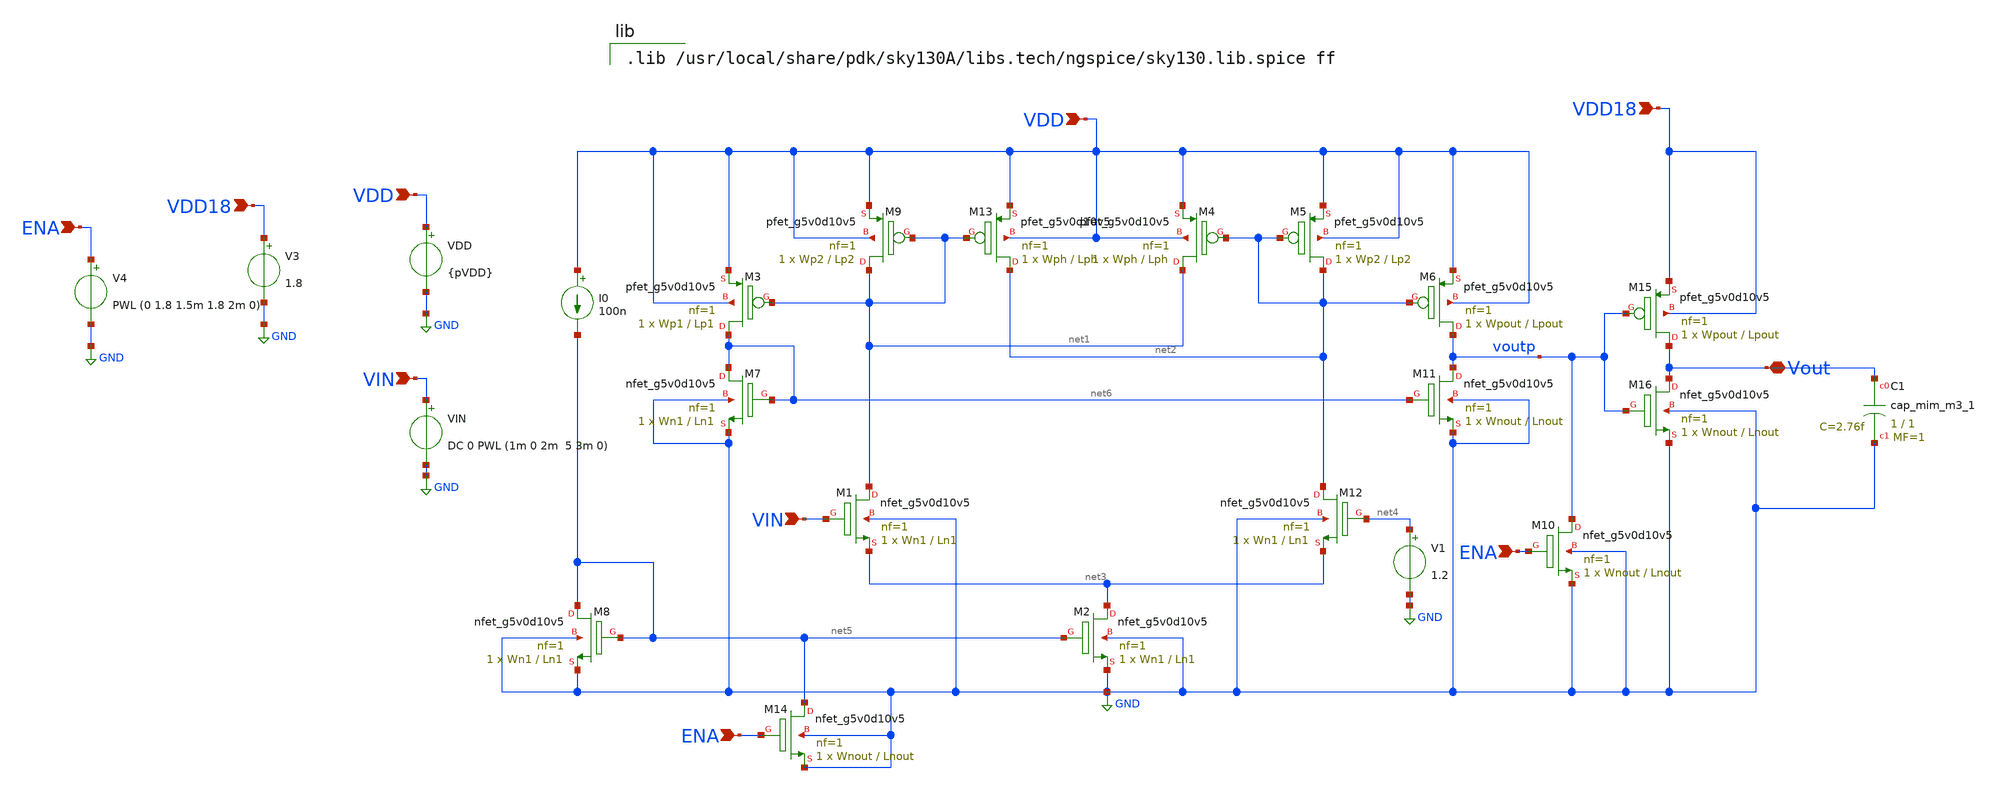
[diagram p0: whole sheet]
** sch_path: xschem/Comparador_Final.sch
**.subckt Comparador_Final VDD VDD Vout VIN VIN VDD18 VDD18 ENA ENA ENA
*.ipin VDD
*.ipin VDD
*.iopin Vout
*.ipin VIN
*.ipin VIN
*.ipin VDD18
*.ipin VDD18
*.ipin ENA
*.ipin ENA
*.ipin ENA
V1 net4 GND 1.2
VDD VDD GND {pVDD}
VIN VIN GND DC 0 PWL (1m 0 2m 5 3m 0)
I0 VDD net5 100n
XM3 net6 net1 VDD VDD sky130_fd_pr__pfet_g5v0d10v5 L=Lp1 W=Wp1 nf=1 ad='int((nf+1)/2) * W/nf * 0.29'
+ as='int((nf+2)/2) * W/nf * 0.29' pd='2*int((nf+1)/2) * (W/nf + 0.29)' ps='2*int((nf+2)/2) * (W/nf + 0.29)'
+ nrd='0.29 / W' nrs='0.29 / W' sa=0 sb=0 sd=0 mult=1 m=1
XM9 net1 net1 VDD VDD sky130_fd_pr__pfet_g5v0d10v5 L=Lp2 W=Wp2 nf=1 ad='int((nf+1)/2) * W/nf * 0.29'
+ as='int((nf+2)/2) * W/nf * 0.29' pd='2*int((nf+1)/2) * (W/nf + 0.29)' ps='2*int((nf+2)/2) * (W/nf + 0.29)'
+ nrd='0.29 / W' nrs='0.29 / W' sa=0 sb=0 sd=0 mult=1 m=1
XM13 net2 net1 VDD VDD sky130_fd_pr__pfet_g5v0d10v5 L=Lph W=Wph nf=1 ad='int((nf+1)/2) * W/nf * 0.29'
+ as='int((nf+2)/2) * W/nf * 0.29' pd='2*int((nf+1)/2) * (W/nf + 0.29)' ps='2*int((nf+2)/2) * (W/nf + 0.29)'
+ nrd='0.29 / W' nrs='0.29 / W' sa=0 sb=0 sd=0 mult=1 m=1
XM4 net1 net2 VDD VDD sky130_fd_pr__pfet_g5v0d10v5 L=Lph W=Wph nf=1 ad='int((nf+1)/2) * W/nf * 0.29'
+ as='int((nf+2)/2) * W/nf * 0.29' pd='2*int((nf+1)/2) * (W/nf + 0.29)' ps='2*int((nf+2)/2) * (W/nf + 0.29)'
+ nrd='0.29 / W' nrs='0.29 / W' sa=0 sb=0 sd=0 mult=1 m=1
XM5 net2 net2 VDD VDD sky130_fd_pr__pfet_g5v0d10v5 L=Lp2 W=Wp2 nf=1 ad='int((nf+1)/2) * W/nf * 0.29'
+ as='int((nf+2)/2) * W/nf * 0.29' pd='2*int((nf+1)/2) * (W/nf + 0.29)' ps='2*int((nf+2)/2) * (W/nf + 0.29)'
+ nrd='0.29 / W' nrs='0.29 / W' sa=0 sb=0 sd=0 mult=1 m=1
XM6 voutp net2 VDD VDD sky130_fd_pr__pfet_g5v0d10v5 L=Lpout W=Wpout nf=1 ad='int((nf+1)/2) * W/nf * 0.29'
+ as='int((nf+2)/2) * W/nf * 0.29' pd='2*int((nf+1)/2) * (W/nf + 0.29)' ps='2*int((nf+2)/2) * (W/nf + 0.29)'
+ nrd='0.29 / W' nrs='0.29 / W' sa=0 sb=0 sd=0 mult=1 m=1
XM11 voutp net6 GND GND sky130_fd_pr__nfet_g5v0d10v5 L=Lnout W=Wnout nf=1 ad='int((nf+1)/2) * W/nf * 0.29'
+ as='int((nf+2)/2) * W/nf * 0.29' pd='2*int((nf+1)/2) * (W/nf + 0.29)' ps='2*int((nf+2)/2) * (W/nf + 0.29)'
+ nrd='0.29 / W' nrs='0.29 / W' sa=0 sb=0 sd=0 mult=1 m=1
XM12 net2 net4 net3 GND sky130_fd_pr__nfet_g5v0d10v5 L=Ln1 W=Wn1 nf=1 ad='int((nf+1)/2) * W/nf * 0.29'
+ as='int((nf+2)/2) * W/nf * 0.29' pd='2*int((nf+1)/2) * (W/nf + 0.29)' ps='2*int((nf+2)/2) * (W/nf + 0.29)'
+ nrd='0.29 / W' nrs='0.29 / W' sa=0 sb=0 sd=0 mult=1 m=1
XM2 net3 net5 GND GND sky130_fd_pr__nfet_g5v0d10v5 L=Ln1 W=Wn1 nf=1 ad='int((nf+1)/2) * W/nf * 0.29'
+ as='int((nf+2)/2) * W/nf * 0.29' pd='2*int((nf+1)/2) * (W/nf + 0.29)' ps='2*int((nf+2)/2) * (W/nf + 0.29)'
+ nrd='0.29 / W' nrs='0.29 / W' sa=0 sb=0 sd=0 mult=1 m=1
XM1 net1 VIN net3 GND sky130_fd_pr__nfet_g5v0d10v5 L=Ln1 W=Wn1 nf=1 ad='int((nf+1)/2) * W/nf * 0.29'
+ as='int((nf+2)/2) * W/nf * 0.29' pd='2*int((nf+1)/2) * (W/nf + 0.29)' ps='2*int((nf+2)/2) * (W/nf + 0.29)'
+ nrd='0.29 / W' nrs='0.29 / W' sa=0 sb=0 sd=0 mult=1 m=1
XM7 net6 net6 GND GND sky130_fd_pr__nfet_g5v0d10v5 L=Ln1 W=Wn1 nf=1 ad='int((nf+1)/2) * W/nf * 0.29'
+ as='int((nf+2)/2) * W/nf * 0.29' pd='2*int((nf+1)/2) * (W/nf + 0.29)' ps='2*int((nf+2)/2) * (W/nf + 0.29)'
+ nrd='0.29 / W' nrs='0.29 / W' sa=0 sb=0 sd=0 mult=1 m=1
XM8 net5 net5 GND GND sky130_fd_pr__nfet_g5v0d10v5 L=Ln1 W=Wn1 nf=1 ad='int((nf+1)/2) * W/nf * 0.29'
+ as='int((nf+2)/2) * W/nf * 0.29' pd='2*int((nf+1)/2) * (W/nf + 0.29)' ps='2*int((nf+2)/2) * (W/nf + 0.29)'
+ nrd='0.29 / W' nrs='0.29 / W' sa=0 sb=0 sd=0 mult=1 m=1
V3 VDD18 GND 1.8
XM15 Vout voutp VDD18 VDD18 sky130_fd_pr__pfet_g5v0d10v5 L=Lpout W=Wpout nf=1 ad='int((nf+1)/2) * W/nf * 0.29'
+ as='int((nf+2)/2) * W/nf * 0.29' pd='2*int((nf+1)/2) * (W/nf + 0.29)' ps='2*int((nf+2)/2) * (W/nf + 0.29)'
+ nrd='0.29 / W' nrs='0.29 / W' sa=0 sb=0 sd=0 mult=1 m=1
XM16 Vout voutp GND GND sky130_fd_pr__nfet_g5v0d10v5 L=Lnout W=Wnout nf=1 ad='int((nf+1)/2) * W/nf * 0.29'
+ as='int((nf+2)/2) * W/nf * 0.29' pd='2*int((nf+1)/2) * (W/nf + 0.29)' ps='2*int((nf+2)/2) * (W/nf + 0.29)'
+ nrd='0.29 / W' nrs='0.29 / W' sa=0 sb=0 sd=0 mult=1 m=1
XM10 voutp ENA GND GND sky130_fd_pr__nfet_g5v0d10v5 L=Lnout W=Wnout nf=1 ad='int((nf+1)/2) * W/nf * 0.29'
+ as='int((nf+2)/2) * W/nf * 0.29' pd='2*int((nf+1)/2) * (W/nf + 0.29)' ps='2*int((nf+2)/2) * (W/nf + 0.29)'
+ nrd='0.29 / W' nrs='0.29 / W' sa=0 sb=0 sd=0 mult=1 m=1
XM14 net5 ENA GND GND sky130_fd_pr__nfet_g5v0d10v5 L=Lnout W=Wnout nf=1 ad='int((nf+1)/2) * W/nf * 0.29'
+ as='int((nf+2)/2) * W/nf * 0.29' pd='2*int((nf+1)/2) * (W/nf + 0.29)' ps='2*int((nf+2)/2) * (W/nf + 0.29)'
+ nrd='0.29 / W' nrs='0.29 / W' sa=0 sb=0 sd=0 mult=1 m=1
V4 ENA GND PWL (0 1.8 1.5m 1.8 2m 0)
XC1 Vout GND sky130_fd_pr__cap_mim_m3_1 W=1 L=1 MF=1 m=1
**** begin user architecture code

.param Wn1 = 5 Ln1 = 1
.param Wp1 = 5 Lp1 = 1
.param Wp2 = 2 Lp2 = 2
.param Wph = 10 Lph = 1
.param Wnout = 5 Lnout = 1
.param Wpout = 5 Lpout = 1
.param ptemp = -40
.param pVDD = 3


.temp {ptemp}
.tran 100n 3.2m 0.5m

.control
foreach var2 3 5 5.5
	echo Vdd $var2
	alterparam pvdd = $var2
	foreach var1 -40 25 85
		echo temperature $var1
		alterparam ptemp =$var1
		reset
		run
		*dc Vin 0 2 0.1
		save all
		*plot vout vs time
		meas tran rth find vin when vin=vout CROSS = 1
		meas tran rtl find vin when vin=vout CROSS = 4
		let vhist = 'rth-rtl'
		print vhist
	end
end
.endc


.lib /usr/local/share/pdk/sky130A/libs.tech/ngspice/sky130.lib.spice ff

**** end user architecture code
**.ends
.GLOBAL GND
.end
